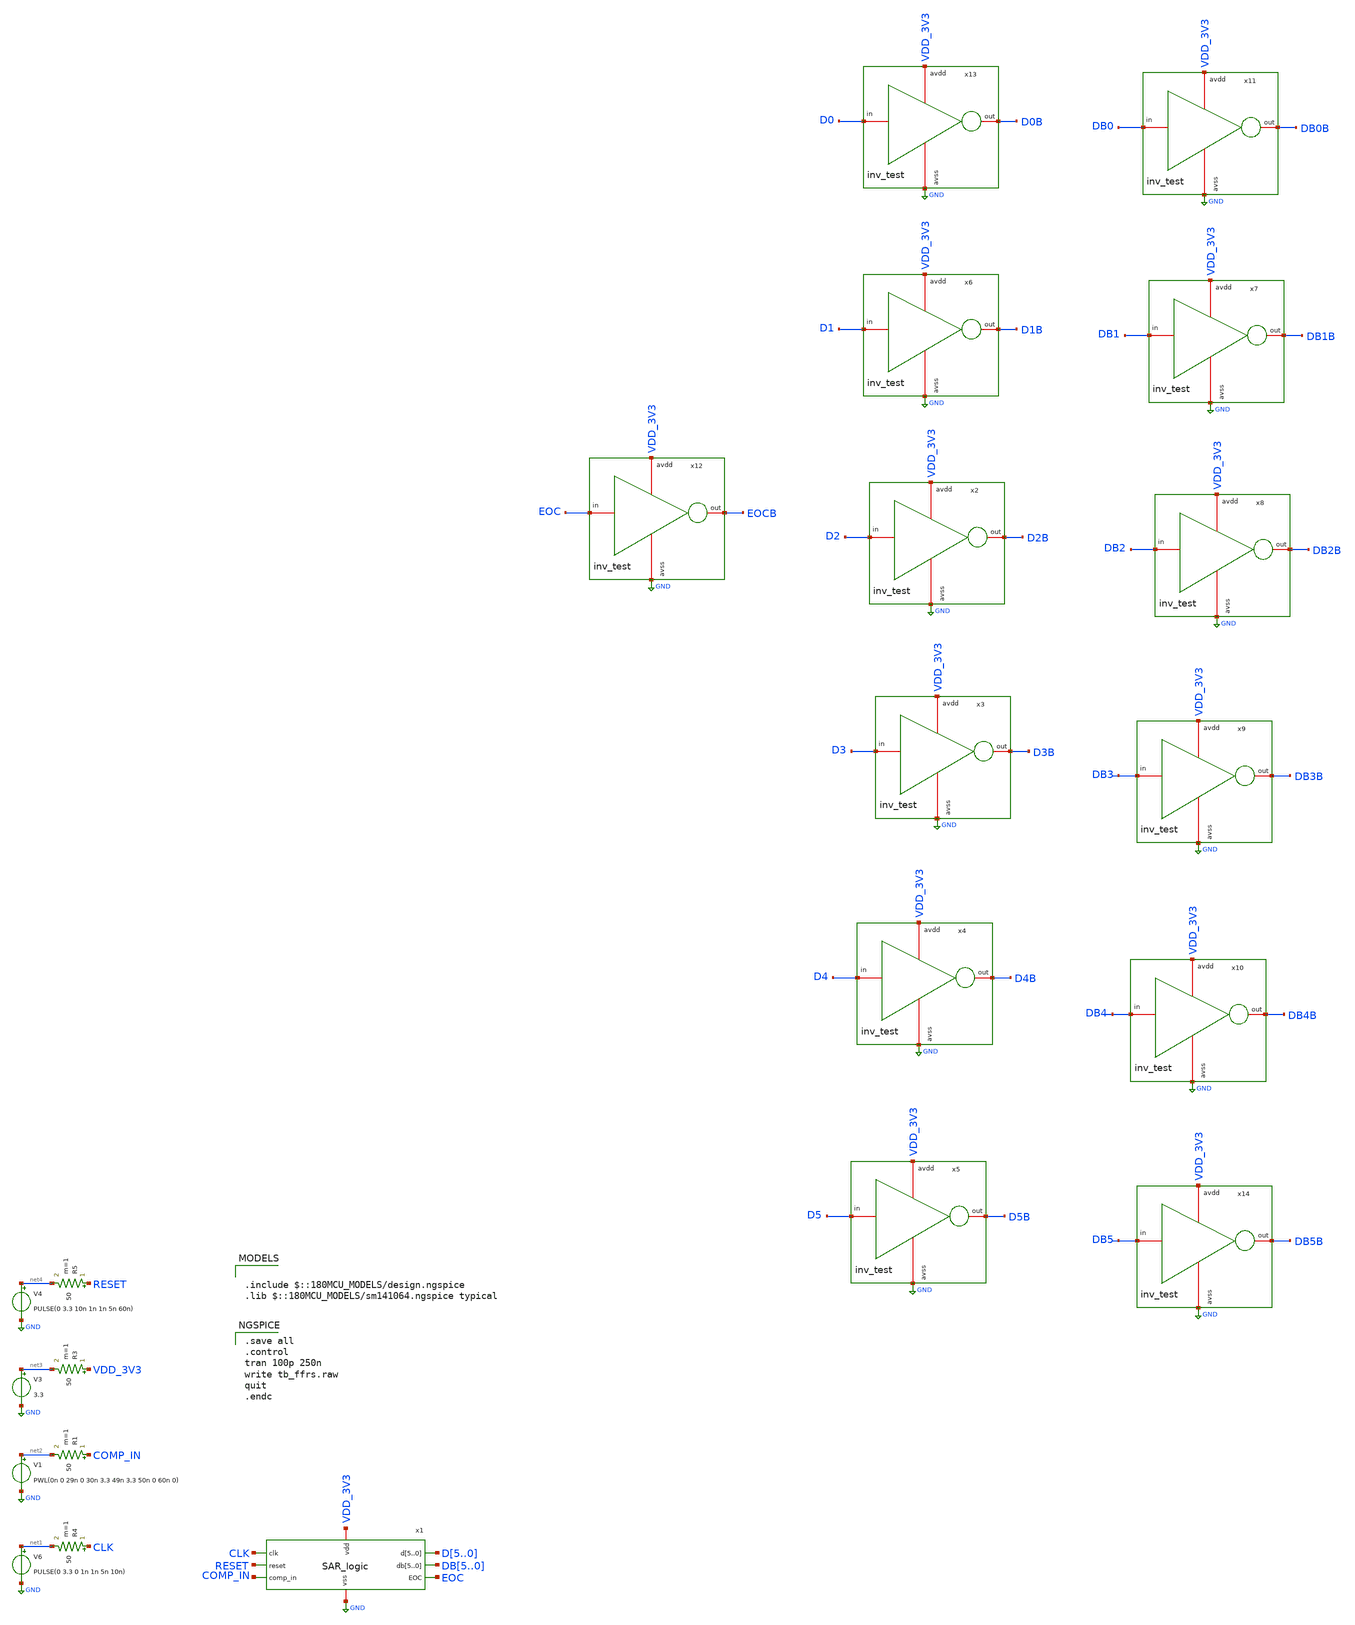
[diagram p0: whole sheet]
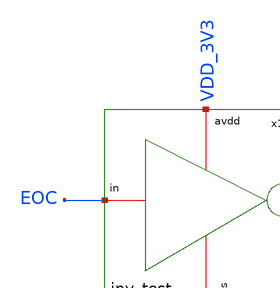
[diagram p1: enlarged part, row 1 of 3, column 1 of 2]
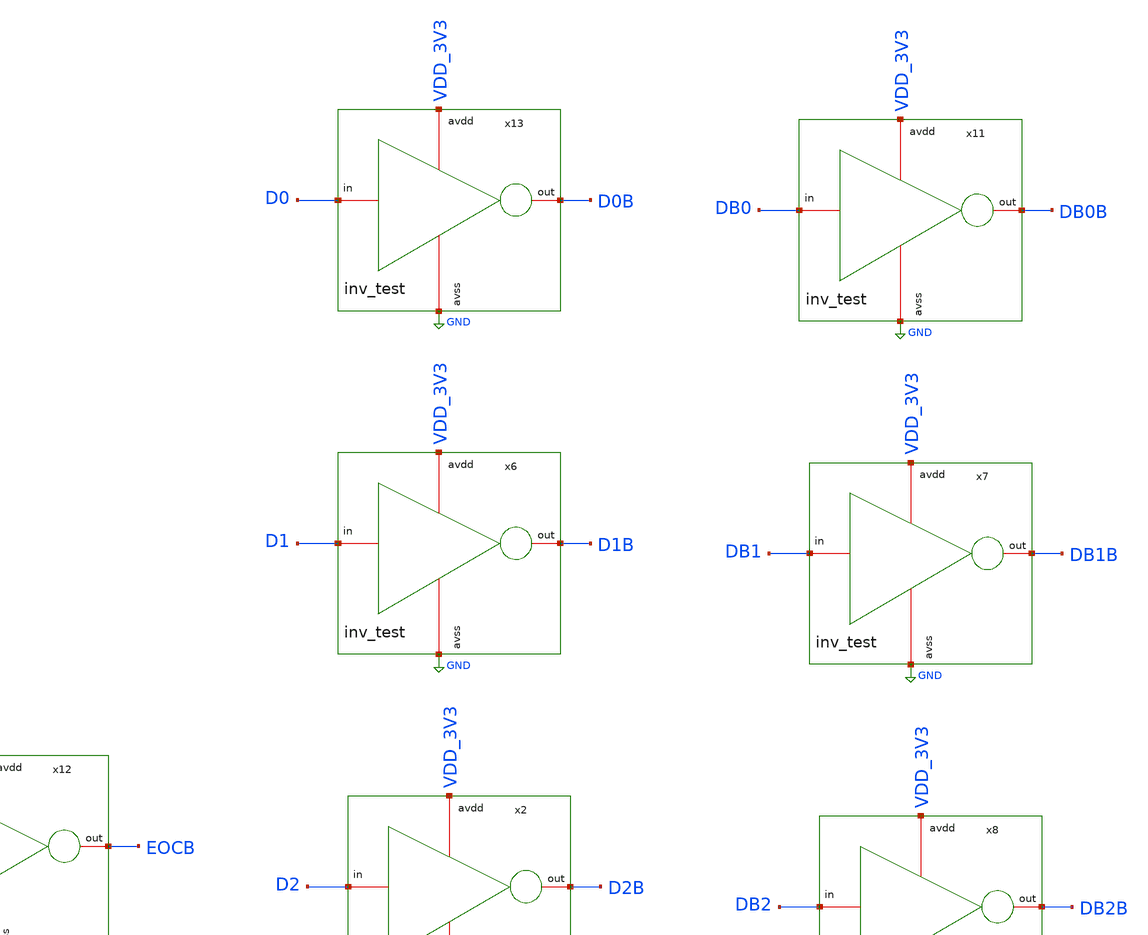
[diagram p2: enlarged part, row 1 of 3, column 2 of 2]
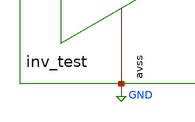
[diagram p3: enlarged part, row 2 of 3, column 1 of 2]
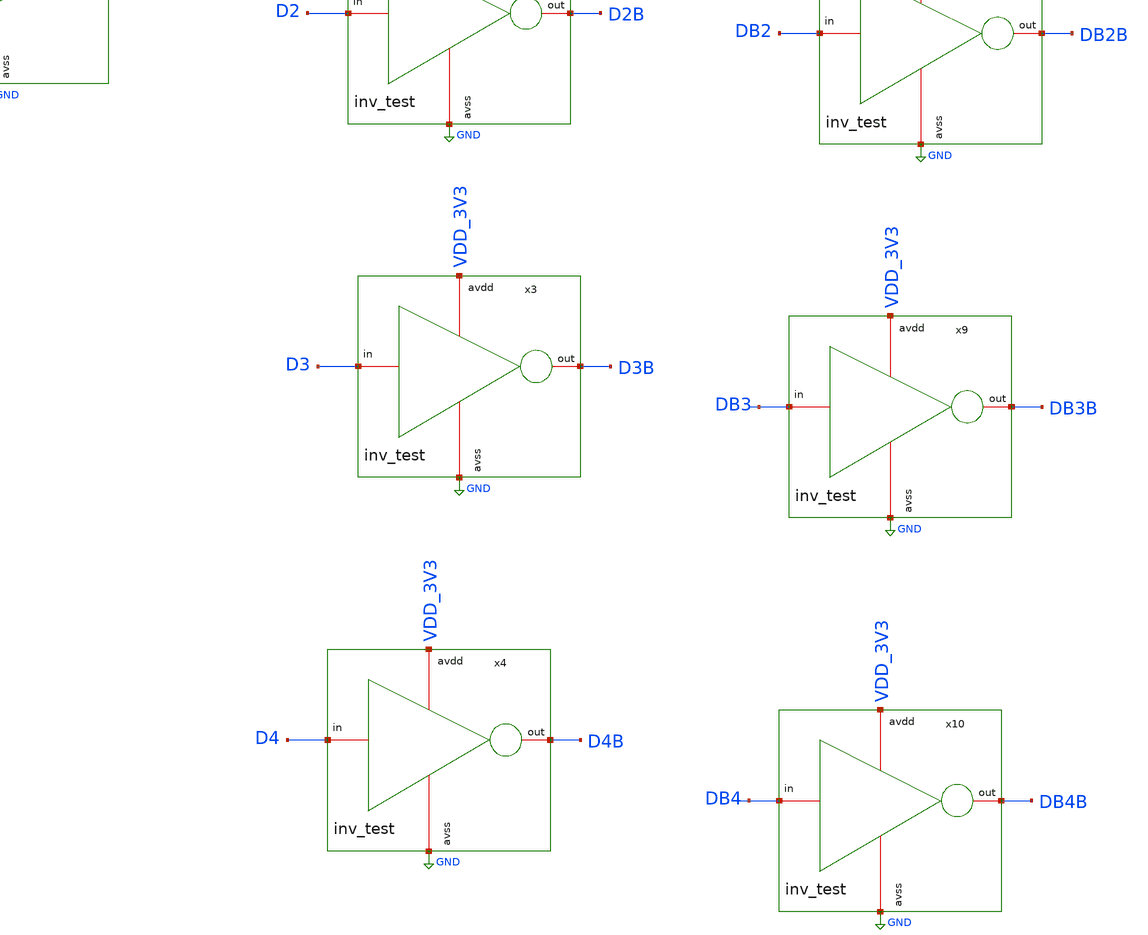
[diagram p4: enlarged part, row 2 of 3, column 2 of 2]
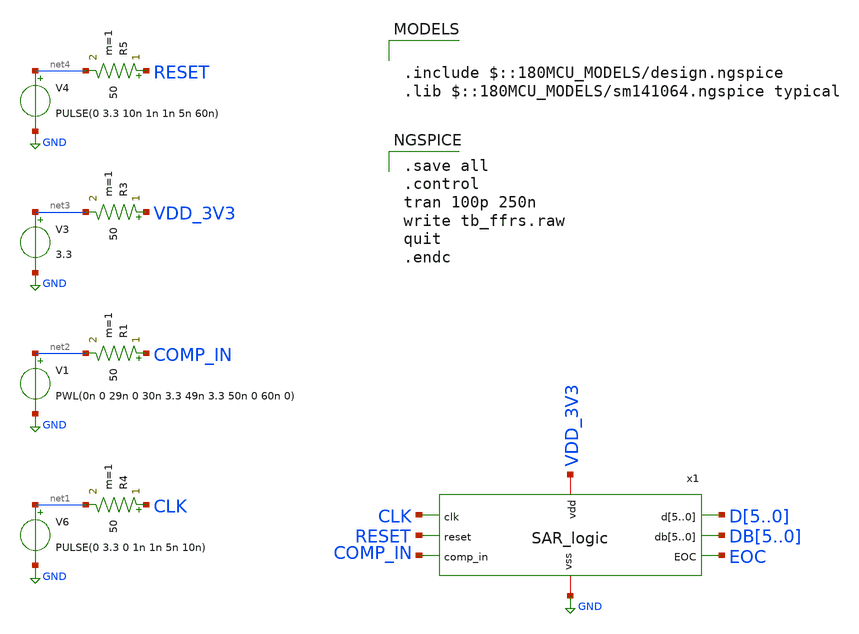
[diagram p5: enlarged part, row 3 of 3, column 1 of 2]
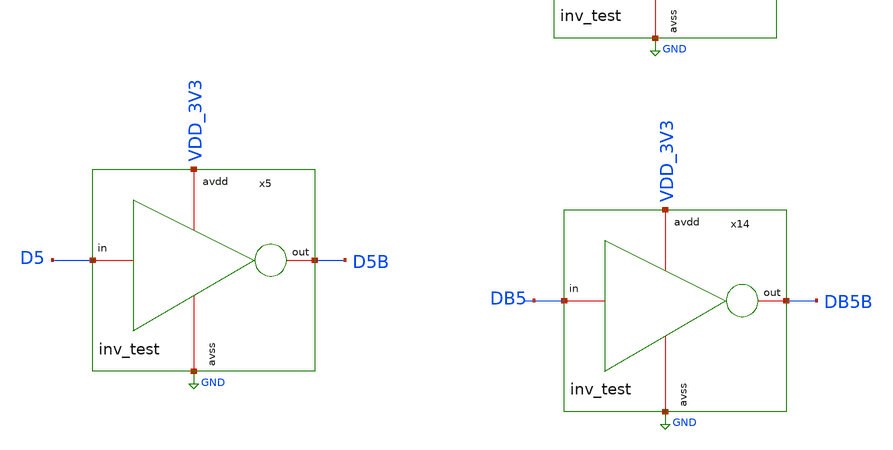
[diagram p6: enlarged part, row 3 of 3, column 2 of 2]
** sch_path: designs/libs/SAR_logic/SAR_logic_inv_output_tb.sch
**.subckt SAR_logic_inv_output_tb
V6 net1 GND PULSE(0 3.3 0 1n 1n 5n 10n)
R4 CLK net1 50 m=1
V1 net2 GND PWL(0n 0 29n 0 30n 3.3 49n 3.3 50n 0 60n 0)
R1 COMP_IN net2 50 m=1
V3 net3 GND 3.3
R3 VDD_3V3 net3 50 m=1
V4 net4 GND PULSE(0 3.3 10n 1n 1n 5n 60n)
R5 RESET net4 50 m=1
x1 VDD_3V3 GND CLK RESET COMP_IN D5 D4 D3 D2 D1 D0 DB5 DB4 DB3 DB2 DB1 DB0 EOC SAR_logic
x2 VDD_3V3 D2 D2B GND inv_test
x3 VDD_3V3 D3 D3B GND inv_test
x4 VDD_3V3 D4 D4B GND inv_test
x5 VDD_3V3 D5 D5B GND inv_test
x6 VDD_3V3 D1 D1B GND inv_test
x7 VDD_3V3 DB1 DB1B GND inv_test
x8 VDD_3V3 DB2 DB2B GND inv_test
x9 VDD_3V3 DB3 DB3B GND inv_test
x10 VDD_3V3 DB4 DB4B GND inv_test
x11 VDD_3V3 DB0 DB0B GND inv_test
x12 VDD_3V3 EOC EOCB GND inv_test
x13 VDD_3V3 D0 D0B GND inv_test
x14 VDD_3V3 DB5 DB5B GND inv_test
**** begin user architecture code

.include $::180MCU_MODELS/design.ngspice
.lib $::180MCU_MODELS/sm141064.ngspice typical


.save all
.control
tran 100p 250n
write tb_ffrs.raw
quit
.endc

**** end user architecture code
**.ends

* expanding   symbol:  libs/SAR_logic/SAR_logic.sym # of pins=8
** sym_path: designs/libs/SAR_logic/SAR_logic.sym
** sch_path: designs/libs/SAR_logic/SAR_logic.sch
.subckt SAR_logic vdd vss clk reset comp_in d5 d4 d3 d2 d1 d0 db5 db4 db3 db2 db1 db0 EOC
*.ipin comp_in
*.iopin vdd
*.iopin vss
*.ipin clk
*.ipin reset
*.opin d5,d4,d3,d2,d1,d0
*.opin EOC
*.opin db5,db4,db3,db2,db1,db0
x1 vdd vss vss clk reset vss ff_init_q net1 tspc_flip_flop
x2 vdd vss ff_init_q clk vss reset ff_5_q net2 tspc_flip_flop
x3 vdd vss ff_5_q clk vss reset ff_4_q net3 tspc_flip_flop
x4 vdd vss ff_4_q clk vss reset ff_3_q net4 tspc_flip_flop
x5 vdd vss ff_3_q clk vss reset ff_2_q net5 tspc_flip_flop
x6 vdd vss ff_2_q clk vss reset ff_1_q net6 tspc_flip_flop
x7 vdd vss ff_1_q clk vss reset ff_0_q net7 tspc_flip_flop
x8 vdd vss ff_0_q clk vss reset EOC net8 tspc_flip_flop
x9 vdd vss comp_in d4 ff_5_q reset d5 db5 tspc_flip_flop
x10 vdd vss comp_in d3 ff_4_q reset d4 db4 tspc_flip_flop
x11 vdd vss comp_in d2 ff_3_q reset d3 db3 tspc_flip_flop
x12 vdd vss comp_in d1 ff_2_q reset d2 db2 tspc_flip_flop
x13 vdd vss comp_in d0 ff_1_q reset d1 db1 tspc_flip_flop
x14 vdd vss comp_in d_end ff_0_q reset d0 db0 tspc_flip_flop
x15 vdd vss vss vss EOC reset d_end net9 tspc_flip_flop
.ends


* expanding   symbol:  libs/WK_Kadam/inv_test.sym # of pins=4
** sym_path: libs/WK_Kadam/inv_test.sym
** sch_path: libs/WK_Kadam/inv_test.sch
.subckt inv_test avdd in out avss
*.iopin avdd
*.iopin avss
*.iopin in
*.iopin out
XM3 out in avss avss nfet_03v3 L=0.28u W=1u nf=1 ad='int((nf+1)/2) * W/nf * 0.18u' as='int((nf+2)/2) * W/nf * 0.18u'
+ pd='2*int((nf+1)/2) * (W/nf + 0.18u)' ps='2*int((nf+2)/2) * (W/nf + 0.18u)' nrd='0.18u / W' nrs='0.18u / W'
+ sa=0 sb=0 sd=0 m=1
XM4 out in avdd avdd pfet_03v3 L=0.28u W=2.5u nf=1 ad='int((nf+1)/2) * W/nf * 0.18u' as='int((nf+2)/2) * W/nf * 0.18u'
+ pd='2*int((nf+1)/2) * (W/nf + 0.18u)' ps='2*int((nf+2)/2) * (W/nf + 0.18u)' nrd='0.18u / W' nrs='0.18u / W'
+ sa=0 sb=0 sd=0 m=1
.ends


* expanding   symbol:  libs/tspc_flip_flop/tspc_flip_flop.sym # of pins=8
** sym_path: designs/libs/tspc_flip_flop/tspc_flip_flop.sym
** sch_path: designs/libs/tspc_flip_flop/tspc_flip_flop.sch
.subckt tspc_flip_flop vdd vss d clk set reset q qb
*.iopin vdd
*.iopin vss
*.ipin d
*.ipin clk
*.ipin set
*.ipin reset
*.opin q
*.opin qb
XM1 b1 d vss vss nfet_03v3 L=0.28u W=1u nf=1 ad='int((nf+1)/2) * W/nf * 0.18u' as='int((nf+2)/2) * W/nf * 0.18u'
+ pd='2*int((nf+1)/2) * (W/nf + 0.18u)' ps='2*int((nf+2)/2) * (W/nf + 0.18u)' nrd='0.18u / W' nrs='0.18u / W'
+ sa=0 sb=0 sd=0 m=1
XM2 b1 clk net1 net1 pfet_03v3 L=0.28u W=2u nf=1 ad='int((nf+1)/2) * W/nf * 0.18u' as='int((nf+2)/2) * W/nf * 0.18u'
+ pd='2*int((nf+1)/2) * (W/nf + 0.18u)' ps='2*int((nf+2)/2) * (W/nf + 0.18u)' nrd='0.18u / W' nrs='0.18u / W'
+ sa=0 sb=0 sd=0 m=1
XM3 net1 d vdd vdd pfet_03v3 L=0.28u W=2u nf=1 ad='int((nf+1)/2) * W/nf * 0.18u' as='int((nf+2)/2) * W/nf * 0.18u'
+ pd='2*int((nf+1)/2) * (W/nf + 0.18u)' ps='2*int((nf+2)/2) * (W/nf + 0.18u)' nrd='0.18u / W' nrs='0.18u / W'
+ sa=0 sb=0 sd=0 m=1
XM4 b2 clk vdd vdd pfet_03v3 L=0.28u W=2u nf=1 ad='int((nf+1)/2) * W/nf * 0.18u' as='int((nf+2)/2) * W/nf * 0.18u'
+ pd='2*int((nf+1)/2) * (W/nf + 0.18u)' ps='2*int((nf+2)/2) * (W/nf + 0.18u)' nrd='0.18u / W' nrs='0.18u / W'
+ sa=0 sb=0 sd=0 m=1
XM5 b2 b1 net2 vss nfet_03v3 L=0.28u W=1u nf=1 ad='int((nf+1)/2) * W/nf * 0.18u' as='int((nf+2)/2) * W/nf * 0.18u'
+ pd='2*int((nf+1)/2) * (W/nf + 0.18u)' ps='2*int((nf+2)/2) * (W/nf + 0.18u)' nrd='0.18u / W' nrs='0.18u / W'
+ sa=0 sb=0 sd=0 m=1
XM6 net2 clk vss vss nfet_03v3 L=0.28u W=1u nf=1 ad='int((nf+1)/2) * W/nf * 0.18u' as='int((nf+2)/2) * W/nf * 0.18u'
+ pd='2*int((nf+1)/2) * (W/nf + 0.18u)' ps='2*int((nf+2)/2) * (W/nf + 0.18u)' nrd='0.18u / W' nrs='0.18u / W'
+ sa=0 sb=0 sd=0 m=1
XM7 net4 b2 vss vss nfet_03v3 L=0.28u W=1u nf=1 ad='int((nf+1)/2) * W/nf * 0.18u' as='int((nf+2)/2) * W/nf * 0.18u'
+ pd='2*int((nf+1)/2) * (W/nf + 0.18u)' ps='2*int((nf+2)/2) * (W/nf + 0.18u)' nrd='0.18u / W' nrs='0.18u / W'
+ sa=0 sb=0 sd=0 m=1
XM8 b3 clk net4 vss nfet_03v3 L=0.28u W=1u nf=1 ad='int((nf+1)/2) * W/nf * 0.18u' as='int((nf+2)/2) * W/nf * 0.18u'
+ pd='2*int((nf+1)/2) * (W/nf + 0.18u)' ps='2*int((nf+2)/2) * (W/nf + 0.18u)' nrd='0.18u / W' nrs='0.18u / W'
+ sa=0 sb=0 sd=0 m=1
XM9 b3 set net3 net3 pfet_03v3 L=0.28u W=2u nf=1 ad='int((nf+1)/2) * W/nf * 0.18u' as='int((nf+2)/2) * W/nf * 0.18u'
+ pd='2*int((nf+1)/2) * (W/nf + 0.18u)' ps='2*int((nf+2)/2) * (W/nf + 0.18u)' nrd='0.18u / W' nrs='0.18u / W'
+ sa=0 sb=0 sd=0 m=1
XM10 net3 b2 vdd vdd pfet_03v3 L=0.28u W=2u nf=1 ad='int((nf+1)/2) * W/nf * 0.18u' as='int((nf+2)/2) * W/nf * 0.18u'
+ pd='2*int((nf+1)/2) * (W/nf + 0.18u)' ps='2*int((nf+2)/2) * (W/nf + 0.18u)' nrd='0.18u / W' nrs='0.18u / W'
+ sa=0 sb=0 sd=0 m=1
XM11 b3 net5 vdd vdd pfet_03v3 L=0.28u W=2u nf=1 ad='int((nf+1)/2) * W/nf * 0.18u' as='int((nf+2)/2) * W/nf * 0.18u'
+ pd='2*int((nf+1)/2) * (W/nf + 0.18u)' ps='2*int((nf+2)/2) * (W/nf + 0.18u)' nrd='0.18u / W' nrs='0.18u / W'
+ sa=0 sb=0 sd=0 m=1
XM12 b3 set vss vss nfet_03v3 L=0.28u W=1u nf=1 ad='int((nf+1)/2) * W/nf * 0.18u' as='int((nf+2)/2) * W/nf * 0.18u'
+ pd='2*int((nf+1)/2) * (W/nf + 0.18u)' ps='2*int((nf+2)/2) * (W/nf + 0.18u)' nrd='0.18u / W' nrs='0.18u / W'
+ sa=0 sb=0 sd=0 m=1
XM13 q b3 vdd vdd pfet_03v3 L=0.28u W=2u nf=1 ad='int((nf+1)/2) * W/nf * 0.18u' as='int((nf+2)/2) * W/nf * 0.18u'
+ pd='2*int((nf+1)/2) * (W/nf + 0.18u)' ps='2*int((nf+2)/2) * (W/nf + 0.18u)' nrd='0.18u / W' nrs='0.18u / W'
+ sa=0 sb=0 sd=0 m=1
XM14 q b3 vss vss nfet_03v3 L=0.28u W=1u nf=1 ad='int((nf+1)/2) * W/nf * 0.18u' as='int((nf+2)/2) * W/nf * 0.18u'
+ pd='2*int((nf+1)/2) * (W/nf + 0.18u)' ps='2*int((nf+2)/2) * (W/nf + 0.18u)' nrd='0.18u / W' nrs='0.18u / W'
+ sa=0 sb=0 sd=0 m=1
XM15 net5 reset vdd vdd pfet_03v3 L=0.28u W=2u nf=1 ad='int((nf+1)/2) * W/nf * 0.18u' as='int((nf+2)/2) * W/nf * 0.18u'
+ pd='2*int((nf+1)/2) * (W/nf + 0.18u)' ps='2*int((nf+2)/2) * (W/nf + 0.18u)' nrd='0.18u / W' nrs='0.18u / W'
+ sa=0 sb=0 sd=0 m=1
XM16 net5 reset vss vss nfet_03v3 L=0.28u W=1u nf=1 ad='int((nf+1)/2) * W/nf * 0.18u' as='int((nf+2)/2) * W/nf * 0.18u'
+ pd='2*int((nf+1)/2) * (W/nf + 0.18u)' ps='2*int((nf+2)/2) * (W/nf + 0.18u)' nrd='0.18u / W' nrs='0.18u / W'
+ sa=0 sb=0 sd=0 m=1
XM17 qb q vdd vdd pfet_03v3 L=0.28u W=2u nf=1 ad='int((nf+1)/2) * W/nf * 0.18u' as='int((nf+2)/2) * W/nf * 0.18u'
+ pd='2*int((nf+1)/2) * (W/nf + 0.18u)' ps='2*int((nf+2)/2) * (W/nf + 0.18u)' nrd='0.18u / W' nrs='0.18u / W'
+ sa=0 sb=0 sd=0 m=1
XM18 qb q vss vss nfet_03v3 L=0.28u W=1u nf=1 ad='int((nf+1)/2) * W/nf * 0.18u' as='int((nf+2)/2) * W/nf * 0.18u'
+ pd='2*int((nf+1)/2) * (W/nf + 0.18u)' ps='2*int((nf+2)/2) * (W/nf + 0.18u)' nrd='0.18u / W' nrs='0.18u / W'
+ sa=0 sb=0 sd=0 m=1
.ends

.GLOBAL GND
.end
